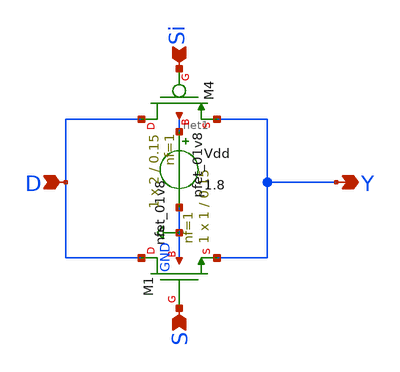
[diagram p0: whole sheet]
** sch_path: Circuit Files/circuits/circuits/Transmission_gates.sch
**.subckt Transmission_gates D Y Si S
*.ipin D
*.opin Y
*.ipin Si
*.ipin S
XM1 D S Y GND sky130_fd_pr__nfet_01v8 L=0.15 W=1 nf=1 ad='int((nf+1)/2) * W/nf * 0.29' as='int((nf+2)/2) * W/nf * 0.29'
+ pd='2*int((nf+1)/2) * (W/nf + 0.29)' ps='2*int((nf+2)/2) * (W/nf + 0.29)' nrd='0.29 / W' nrs='0.29 / W'
+ sa=0 sb=0 sd=0 mult=1 m=1
XM4 D Si Y net1 sky130_fd_pr__pfet_01v8 L=0.15 W=2 nf=1 ad='int((nf+1)/2) * W/nf * 0.29' as='int((nf+2)/2) * W/nf * 0.29'
+ pd='2*int((nf+1)/2) * (W/nf + 0.29)' ps='2*int((nf+2)/2) * (W/nf + 0.29)' nrd='0.29 / W' nrs='0.29 / W'
+ sa=0 sb=0 sd=0 mult=1 m=1
Vdd net1 GND 1.8
**.ends
.GLOBAL GND
.end
